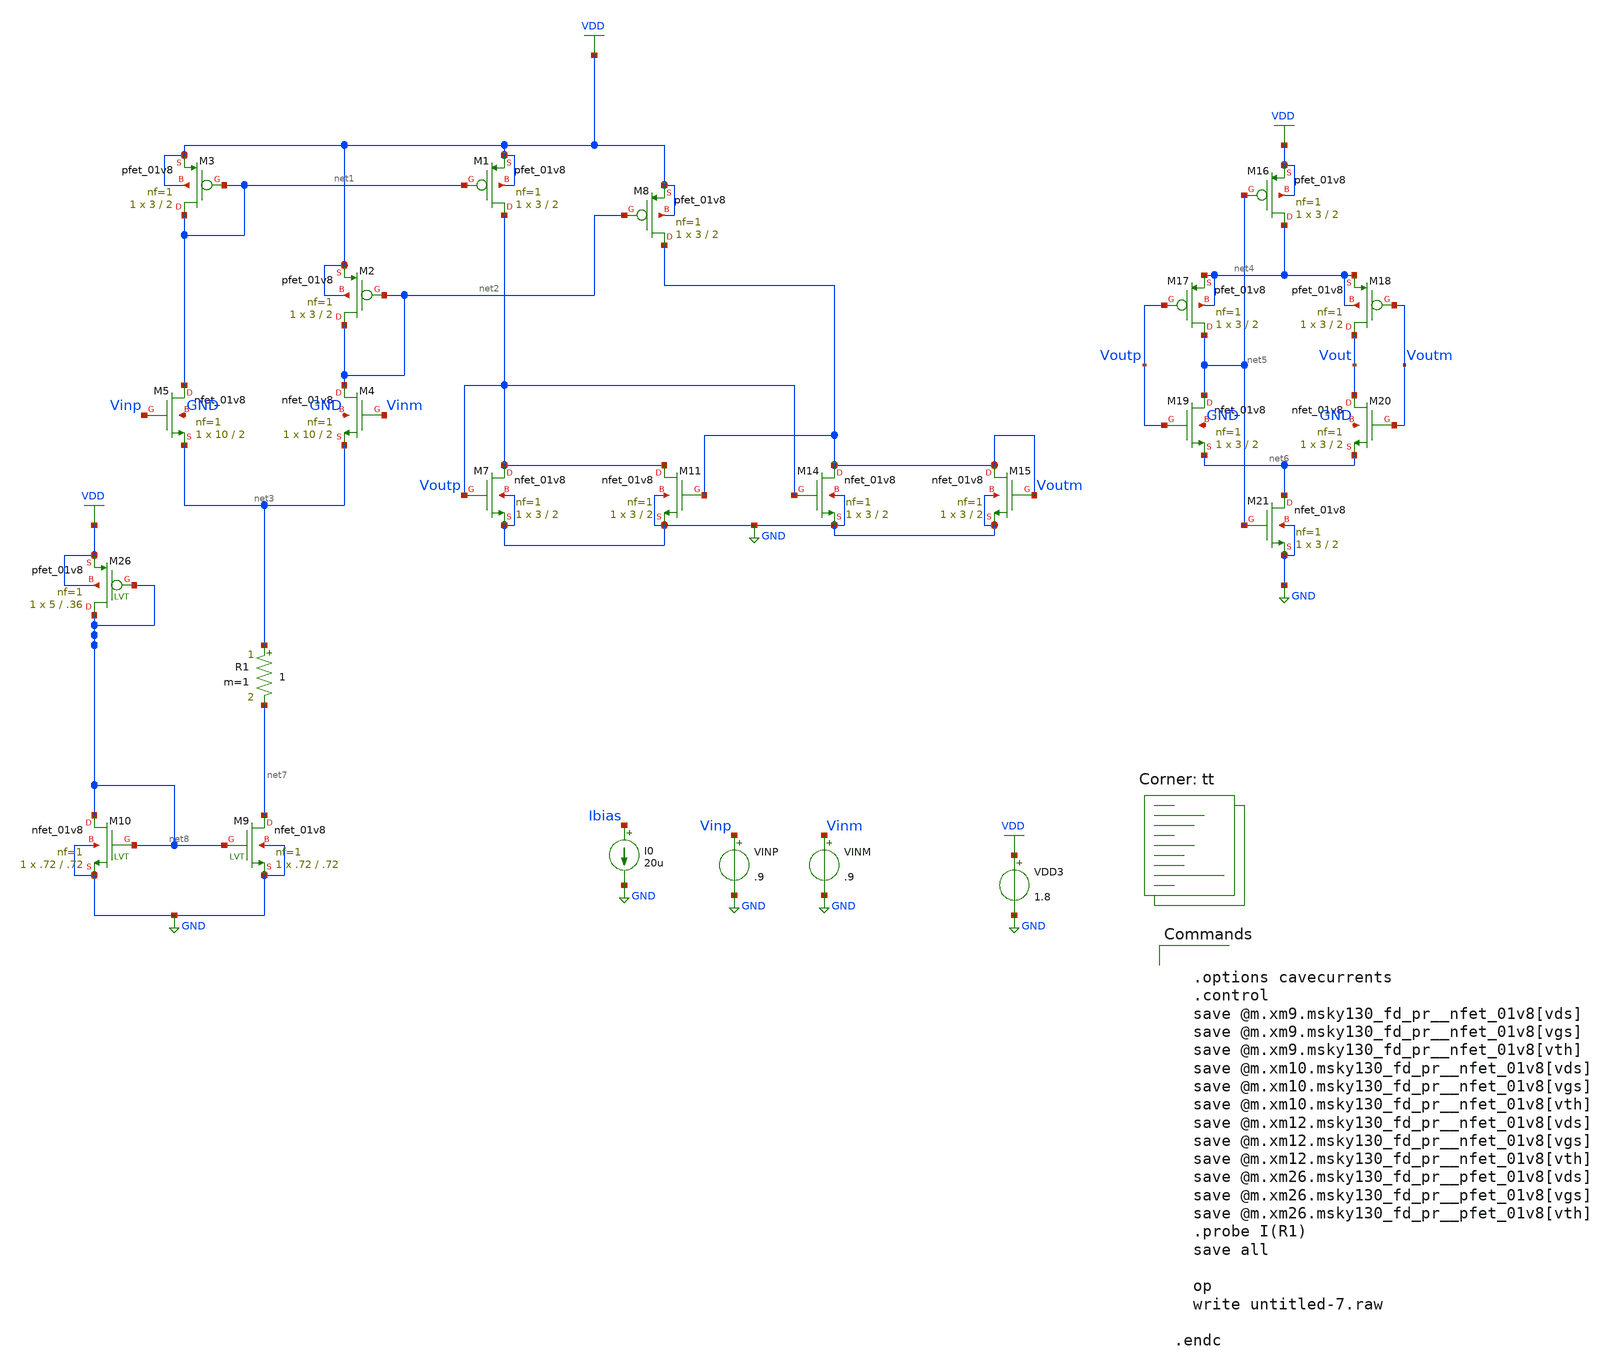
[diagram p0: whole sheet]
** sch_path: untitled-7.sch
**.subckt untitled-7
XM3 net1 net1 VDD VDD sky130_fd_pr__pfet_01v8 L=2 W=3 nf=1 ad='int((nf+1)/2) * W/nf * 0.29' as='int((nf+2)/2) * W/nf * 0.29'
+ pd='2*int((nf+1)/2) * (W/nf + 0.29)' ps='2*int((nf+2)/2) * (W/nf + 0.29)' nrd='0.29 / W' nrs='0.29 / W'
+ sa=0 sb=0 sd=0 mult=1 m=1
XM1 Voutp net1 VDD VDD sky130_fd_pr__pfet_01v8 L=2 W=3 nf=1 ad='int((nf+1)/2) * W/nf * 0.29' as='int((nf+2)/2) * W/nf * 0.29'
+ pd='2*int((nf+1)/2) * (W/nf + 0.29)' ps='2*int((nf+2)/2) * (W/nf + 0.29)' nrd='0.29 / W' nrs='0.29 / W'
+ sa=0 sb=0 sd=0 mult=1 m=1
XM2 net2 net2 VDD VDD sky130_fd_pr__pfet_01v8 L=2 W=3 nf=1 ad='int((nf+1)/2) * W/nf * 0.29' as='int((nf+2)/2) * W/nf * 0.29'
+ pd='2*int((nf+1)/2) * (W/nf + 0.29)' ps='2*int((nf+2)/2) * (W/nf + 0.29)' nrd='0.29 / W' nrs='0.29 / W'
+ sa=0 sb=0 sd=0 mult=1 m=1
XM4 net2 Vinm net3 GND sky130_fd_pr__nfet_01v8 L=2 W=10 nf=1 ad='int((1 + 1)/2) * 10 / 1 * 0.29' as='int((1 + 2)/2) * 10 / 1 * 0.29'
+ pd='2*int((1 + 1)/2) * (10 / 1 + 0.29)' ps='2*int((1 + 2)/2) * (10 / 1 + 0.29)' nrd='0.29 / 10 ' nrs='0.29 / 10 '
+ sa=0 sb=0 sd=0 mult=1 m=1
XM5 net1 Vinp net3 GND sky130_fd_pr__nfet_01v8 L=2 W=10 nf=1 ad='int((1 + 1)/2) * 10 / 1 * 0.29' as='int((1 + 2)/2) * 10 / 1 * 0.29'
+ pd='2*int((1 + 1)/2) * (10 / 1 + 0.29)' ps='2*int((1 + 2)/2) * (10 / 1 + 0.29)' nrd='0.29 / 10 ' nrs='0.29 / 10 '
+ sa=0 sb=0 sd=0 mult=1 m=1
XM7 Voutp Voutp GND GND sky130_fd_pr__nfet_01v8 L=2 W=3 nf=1 ad='int((1 + 1)/2) * 3 / 1 * 0.29' as='int((1 + 2)/2) * 3 / 1 * 0.29'
+ pd='2*int((1 + 1)/2) * (3 / 1 + 0.29)' ps='2*int((1 + 2)/2) * (3 / 1 + 0.29)' nrd='0.29 / 3 ' nrs='0.29 / 3 '
+ sa=0 sb=0 sd=0 mult=1 m=1
XM8 Voutm net2 VDD VDD sky130_fd_pr__pfet_01v8 L=2 W=3 nf=1 ad='int((nf+1)/2) * W/nf * 0.29' as='int((nf+2)/2) * W/nf * 0.29'
+ pd='2*int((nf+1)/2) * (W/nf + 0.29)' ps='2*int((nf+2)/2) * (W/nf + 0.29)' nrd='0.29 / W' nrs='0.29 / W'
+ sa=0 sb=0 sd=0 mult=1 m=1
XM11 Voutp Voutm GND GND sky130_fd_pr__nfet_01v8 L=2 W=3 nf=1 ad='int((1 + 1)/2) * 3 / 1 * 0.29' as='int((1 + 2)/2) * 3 / 1 * 0.29'
+ pd='2*int((1 + 1)/2) * (3 / 1 + 0.29)' ps='2*int((1 + 2)/2) * (3 / 1 + 0.29)' nrd='0.29 / 3 ' nrs='0.29 / 3 '
+ sa=0 sb=0 sd=0 mult=1 m=1
XM14 Voutm Voutp GND GND sky130_fd_pr__nfet_01v8 L=2 W=3 nf=1 ad='int((1 + 1)/2) * 3 / 1 * 0.29' as='int((1 + 2)/2) * 3 / 1 * 0.29'
+ pd='2*int((1 + 1)/2) * (3 / 1 + 0.29)' ps='2*int((1 + 2)/2) * (3 / 1 + 0.29)' nrd='0.29 / 3 ' nrs='0.29 / 3 '
+ sa=0 sb=0 sd=0 mult=1 m=1
XM15 Voutm Voutm GND GND sky130_fd_pr__nfet_01v8 L=2 W=3 nf=1 ad='int((1 + 1)/2) * 3 / 1 * 0.29' as='int((1 + 2)/2) * 3 / 1 * 0.29'
+ pd='2*int((1 + 1)/2) * (3 / 1 + 0.29)' ps='2*int((1 + 2)/2) * (3 / 1 + 0.29)' nrd='0.29 / 3 ' nrs='0.29 / 3 '
+ sa=0 sb=0 sd=0 mult=1 m=1
XM16 net4 net5 VDD VDD sky130_fd_pr__pfet_01v8 L=2 W=3 nf=1 ad='int((nf+1)/2) * W/nf * 0.29' as='int((nf+2)/2) * W/nf * 0.29'
+ pd='2*int((nf+1)/2) * (W/nf + 0.29)' ps='2*int((nf+2)/2) * (W/nf + 0.29)' nrd='0.29 / W' nrs='0.29 / W'
+ sa=0 sb=0 sd=0 mult=1 m=1
XM17 net5 Voutp net4 net4 sky130_fd_pr__pfet_01v8 L=2 W=3 nf=1 ad='int((nf+1)/2) * W/nf * 0.29' as='int((nf+2)/2) * W/nf * 0.29'
+ pd='2*int((nf+1)/2) * (W/nf + 0.29)' ps='2*int((nf+2)/2) * (W/nf + 0.29)' nrd='0.29 / W' nrs='0.29 / W'
+ sa=0 sb=0 sd=0 mult=1 m=1
XM18 Vout Voutm net4 net4 sky130_fd_pr__pfet_01v8 L=2 W=3 nf=1 ad='int((nf+1)/2) * W/nf * 0.29' as='int((nf+2)/2) * W/nf * 0.29'
+ pd='2*int((nf+1)/2) * (W/nf + 0.29)' ps='2*int((nf+2)/2) * (W/nf + 0.29)' nrd='0.29 / W' nrs='0.29 / W'
+ sa=0 sb=0 sd=0 mult=1 m=1
XM19 net5 Voutp net6 GND sky130_fd_pr__nfet_01v8 L=2 W=3 nf=1 ad='int((1 + 1)/2) * 3 / 1 * 0.29' as='int((1 + 2)/2) * 3 / 1 * 0.29'
+ pd='2*int((1 + 1)/2) * (3 / 1 + 0.29)' ps='2*int((1 + 2)/2) * (3 / 1 + 0.29)' nrd='0.29 / 3 ' nrs='0.29 / 3 '
+ sa=0 sb=0 sd=0 mult=1 m=1
XM20 Vout Voutm net6 GND sky130_fd_pr__nfet_01v8 L=2 W=3 nf=1 ad='int((1 + 1)/2) * 3 / 1 * 0.29' as='int((1 + 2)/2) * 3 / 1 * 0.29'
+ pd='2*int((1 + 1)/2) * (3 / 1 + 0.29)' ps='2*int((1 + 2)/2) * (3 / 1 + 0.29)' nrd='0.29 / 3 ' nrs='0.29 / 3 '
+ sa=0 sb=0 sd=0 mult=1 m=1
XM21 net6 net5 GND GND sky130_fd_pr__nfet_01v8 L=2 W=3 nf=1 ad='int((1 + 1)/2) * 3 / 1 * 0.29' as='int((1 + 2)/2) * 3 / 1 * 0.29'
+ pd='2*int((1 + 1)/2) * (3 / 1 + 0.29)' ps='2*int((1 + 2)/2) * (3 / 1 + 0.29)' nrd='0.29 / 3 ' nrs='0.29 / 3 '
+ sa=0 sb=0 sd=0 mult=1 m=1
VDD3 VDD GND 1.8
VINP Vinp GND .9
VINM Vinm GND .9
I0 Ibias GND 20u
XM9 net7 net8 GND GND sky130_fd_pr__nfet_01v8 L=.72 W=.72 nf=1 ad='int((1 + 1)/2) * .72 / 1 * 0.29' as='int((1 + 2)/2) * .72 / 1 * 0.29'
+ pd='2*int((1 + 1)/2) * (.72 / 1 + 0.29)' ps='2*int((1 + 2)/2) * (.72 / 1 + 0.29)' nrd='0.29 / .72 ' nrs='0.29 / .72 '
+ sa=0 sb=0 sd=0 mult=1 m=1
XM10 net8 net8 GND GND sky130_fd_pr__nfet_01v8 L=.72 W=.72 nf=1 ad='int((1 + 1)/2) * .72 / 1 * 0.29'
+ as='int((1 + 2)/2) * .72 / 1 * 0.29' pd='2*int((1 + 1)/2) * (.72 / 1 + 0.29)' ps='2*int((1 + 2)/2) * (.72 / 1 + 0.29)'
+ nrd='0.29 / .72 ' nrs='0.29 / .72 ' sa=0 sb=0 sd=0 mult=1 m=1
XM26 net8 net8 VDD VDD sky130_fd_pr__pfet_01v8 L=.36 W=5 nf=1 ad='int((1 + 1)/2) * 5 / 1 * 0.29' as='int((1 + 2)/2) * 5 / 1 * 0.29'
+ pd='2*int((1 + 1)/2) * (5 / 1 + 0.29)' ps='2*int((1 + 2)/2) * (5 / 1 + 0.29)' nrd='0.29 / 5 ' nrs='0.29 / 5 '
+ sa=0 sb=0 sd=0 mult=1 m=1
R1 net3 net7 1 m=1
**** begin user architecture code


  .options cavecurrents
  .control
  save @m.xm9.msky130_fd_pr__nfet_01v8[vds]
  save @m.xm9.msky130_fd_pr__nfet_01v8[vgs]
  save @m.xm9.msky130_fd_pr__nfet_01v8[vth]
  save @m.xm10.msky130_fd_pr__nfet_01v8[vds]
  save @m.xm10.msky130_fd_pr__nfet_01v8[vgs]
  save @m.xm10.msky130_fd_pr__nfet_01v8[vth]
  save @m.xm12.msky130_fd_pr__nfet_01v8[vds]
  save @m.xm12.msky130_fd_pr__nfet_01v8[vgs]
  save @m.xm12.msky130_fd_pr__nfet_01v8[vth]
  save @m.xm26.msky130_fd_pr__pfet_01v8[vds]
  save @m.xm26.msky130_fd_pr__pfet_01v8[vgs]
  save @m.xm26.msky130_fd_pr__pfet_01v8[vth]
  .probe I(R1)
  save all

  op
  write untitled-7.raw

.endc


.lib $::SKYWATER_MODELS/sky130.lib.spice tt
**** end user architecture code
**.ends
.GLOBAL VDD
.GLOBAL GND
.end
